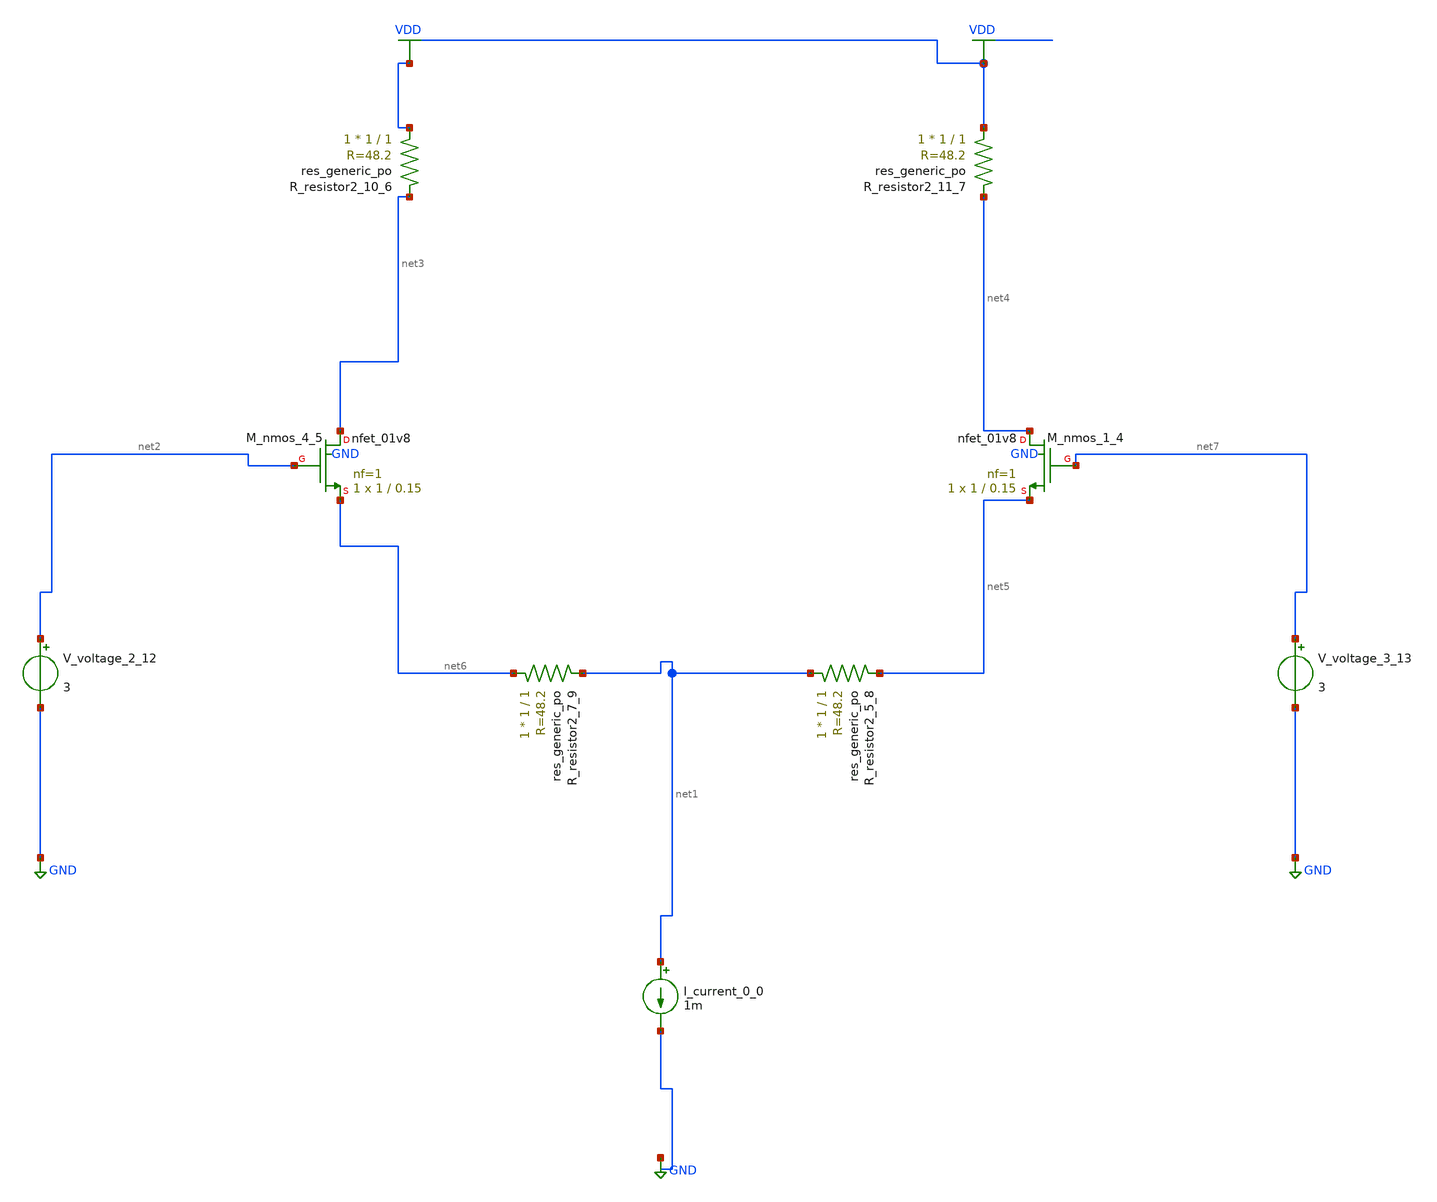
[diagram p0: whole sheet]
** sch_path: schematics/AMSNet/208.sch
**.subckt 208
I_current_0_0 net1 GND 1m
XM_nmos_1_4 net4 net7 net5 GND sky130_fd_pr__nfet_01v8 L=0.15 W=1 nf=1 ad='int((1 + 1)/2) * 1 / 1 * 0.29'
+ as='int((1 + 2)/2) * 1 / 1 * 0.29' pd='2*int((1 + 1)/2) * (1 / 1 + 0.29)' ps='2*int((1 + 2)/2) * (1 / 1 + 0.29)'
+ nrd='0.29 / 1 ' nrs='0.29 / 1 ' sa=0 sb=0 sd=0 mult=1 m=1
XM_nmos_4_5 net3 net2 net6 GND sky130_fd_pr__nfet_01v8 L=0.15 W=1 nf=1 ad='int((1 + 1)/2) * 1 / 1 * 0.29'
+ as='int((1 + 2)/2) * 1 / 1 * 0.29' pd='2*int((1 + 1)/2) * (1 / 1 + 0.29)' ps='2*int((1 + 2)/2) * (1 / 1 + 0.29)'
+ nrd='0.29 / 1 ' nrs='0.29 / 1 ' sa=0 sb=0 sd=0 mult=1 m=1
XR_resistor2_10_6 VDD net3 sky130_fd_pr__res_generic_po W=1 L=1 m=1
XR_resistor2_11_7 VDD net4 sky130_fd_pr__res_generic_po W=1 L=1 m=1
XR_resistor2_5_8 net1 net5 sky130_fd_pr__res_generic_po W=1 L=1 m=1
XR_resistor2_7_9 net6 net1 sky130_fd_pr__res_generic_po W=1 L=1 m=1
V_voltage_2_12 net2 GND 3
V_voltage_3_13 net7 GND 3
**.ends
.GLOBAL GND
.GLOBAL VDD
.end
